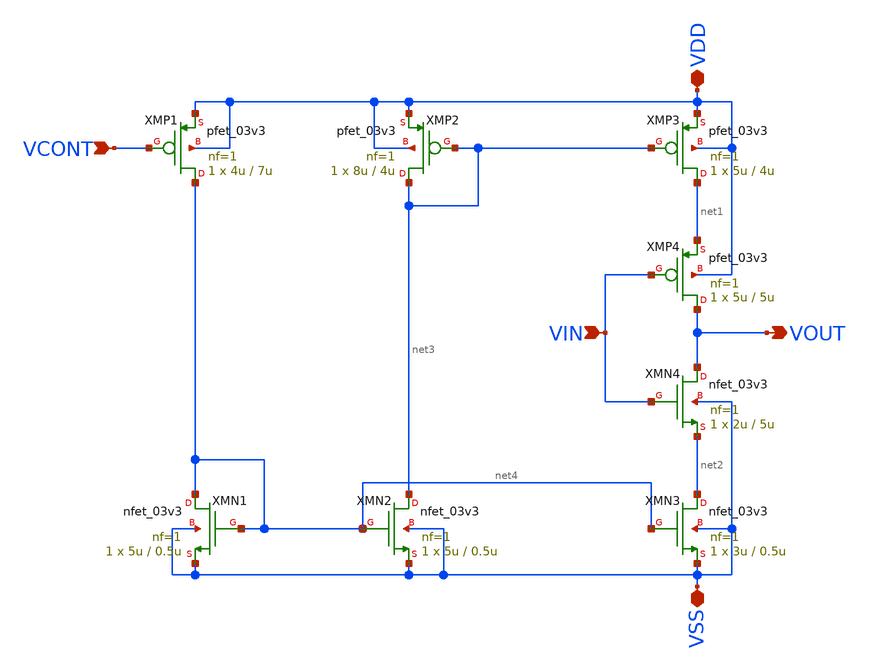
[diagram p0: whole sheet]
** sch_path: xschem/vco/stage_v2p1_GF180.sch
**.subckt stage_v2p1_GF180 VIN VOUT VDD VSS VCONT
*.ipin VIN
*.opin VOUT
*.iopin VDD
*.iopin VSS
*.ipin VCONT
XMN4 VOUT VIN net2 VSS nfet_03v3 L=5u W=2u nf=1 ad='int((nf+1)/2) * W/nf * 0.18u' as='int((nf+2)/2) * W/nf * 0.18u'
+ pd='2*int((nf+1)/2) * (W/nf + 0.18u)' ps='2*int((nf+2)/2) * (W/nf + 0.18u)' nrd='0.18u / W' nrs='0.18u / W'
+ sa=0 sb=0 sd=0 m=1
XMP3 net1 net3 VDD VDD pfet_03v3 L=4u W=5u nf=1 ad='int((nf+1)/2) * W/nf * 0.18u' as='int((nf+2)/2) * W/nf * 0.18u'
+ pd='2*int((nf+1)/2) * (W/nf + 0.18u)' ps='2*int((nf+2)/2) * (W/nf + 0.18u)' nrd='0.18u / W' nrs='0.18u / W'
+ sa=0 sb=0 sd=0 m=1
XMP2 net3 net3 VDD VDD pfet_03v3 L=4u W=8u nf=1 ad='int((nf+1)/2) * W/nf * 0.18u' as='int((nf+2)/2) * W/nf * 0.18u'
+ pd='2*int((nf+1)/2) * (W/nf + 0.18u)' ps='2*int((nf+2)/2) * (W/nf + 0.18u)' nrd='0.18u / W' nrs='0.18u / W'
+ sa=0 sb=0 sd=0 m=1
XMP1 net4 VCONT VDD VDD pfet_03v3 L=7u W=4u nf=1 ad='int((nf+1)/2) * W/nf * 0.18u' as='int((nf+2)/2) * W/nf * 0.18u'
+ pd='2*int((nf+1)/2) * (W/nf + 0.18u)' ps='2*int((nf+2)/2) * (W/nf + 0.18u)' nrd='0.18u / W' nrs='0.18u / W'
+ sa=0 sb=0 sd=0 m=1
XMP4 VOUT VIN net1 VDD pfet_03v3 L=5u W=5u nf=1 ad='int((nf+1)/2) * W/nf * 0.18u' as='int((nf+2)/2) * W/nf * 0.18u'
+ pd='2*int((nf+1)/2) * (W/nf + 0.18u)' ps='2*int((nf+2)/2) * (W/nf + 0.18u)' nrd='0.18u / W' nrs='0.18u / W'
+ sa=0 sb=0 sd=0 m=1
XMN3 net2 net4 VSS VSS nfet_03v3 L=0.5u W=3u nf=1 ad='int((nf+1)/2) * W/nf * 0.18u' as='int((nf+2)/2) * W/nf * 0.18u'
+ pd='2*int((nf+1)/2) * (W/nf + 0.18u)' ps='2*int((nf+2)/2) * (W/nf + 0.18u)' nrd='0.18u / W' nrs='0.18u / W'
+ sa=0 sb=0 sd=0 m=1
XMN2 net3 net4 VSS VSS nfet_03v3 L=0.5u W=5u nf=1 ad='int((nf+1)/2) * W/nf * 0.18u' as='int((nf+2)/2) * W/nf * 0.18u'
+ pd='2*int((nf+1)/2) * (W/nf + 0.18u)' ps='2*int((nf+2)/2) * (W/nf + 0.18u)' nrd='0.18u / W' nrs='0.18u / W'
+ sa=0 sb=0 sd=0 m=1
XMN1 net4 net4 VSS VSS nfet_03v3 L=0.5u W=5u nf=1 ad='int((nf+1)/2) * W/nf * 0.18u' as='int((nf+2)/2) * W/nf * 0.18u'
+ pd='2*int((nf+1)/2) * (W/nf + 0.18u)' ps='2*int((nf+2)/2) * (W/nf + 0.18u)' nrd='0.18u / W' nrs='0.18u / W'
+ sa=0 sb=0 sd=0 m=1
**.ends
.end
